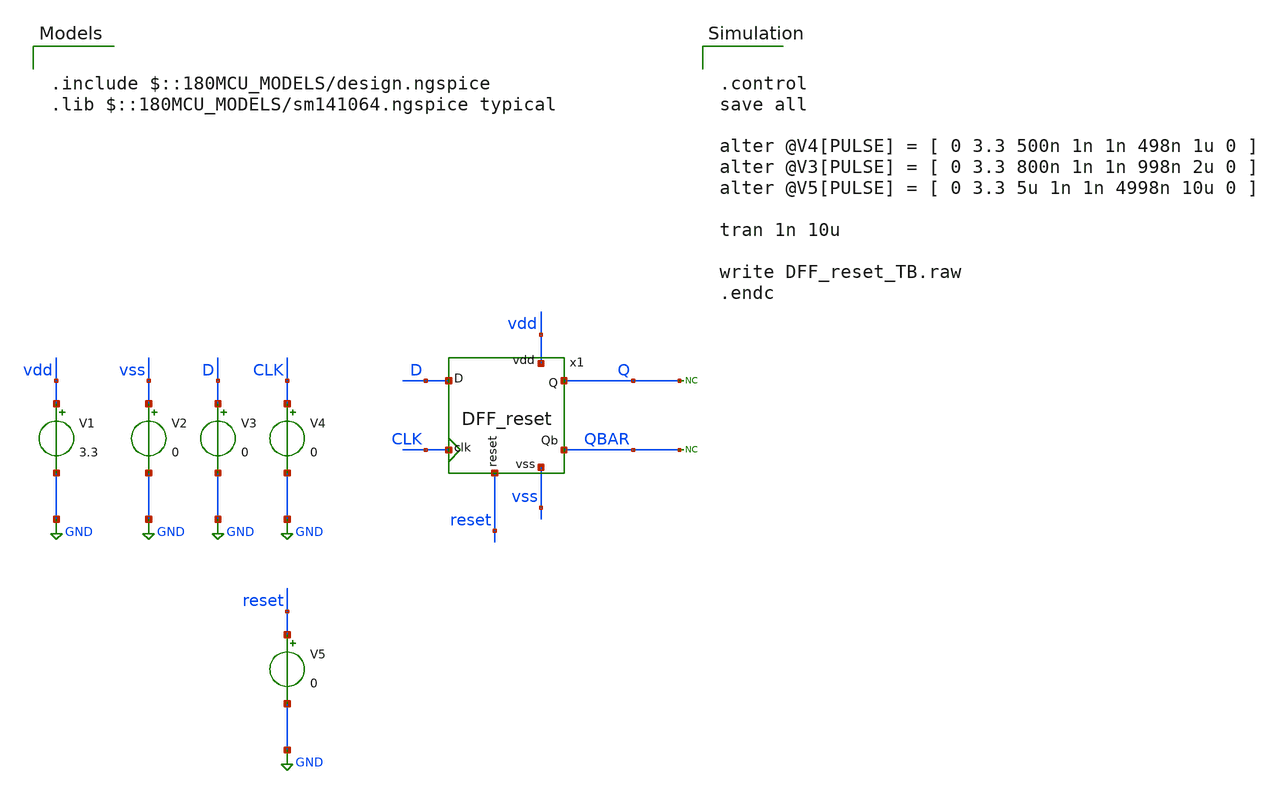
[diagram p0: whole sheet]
** sch_path: designs/libs/xp_tb_analog/tb_DFF_reset/DFF_reset_TB.sch
**.subckt DFF_reset_TB
x1 D Q vdd vss reset QBAR CLK DFF_reset
V1 vdd GND 3.3
V2 vss GND 0
* noconn Q
* noconn QBAR
V3 D GND 0
V4 CLK GND 0
V5 reset GND 0
**** begin user architecture code


.control
save all

alter @V4[PULSE] = [ 0 3.3 500n 1n 1n 498n 1u 0 ]
alter @V3[PULSE] = [ 0 3.3 800n 1n 1n 998n 2u 0 ]
alter @V5[PULSE] = [ 0 3.3 5u 1n 1n 4998n 10u 0 ]

tran 1n 10u

write DFF_reset_TB.raw
.endc



.include $::180MCU_MODELS/design.ngspice
.lib $::180MCU_MODELS/sm141064.ngspice typical

**** end user architecture code
**.ends
.GLOBAL GND
.end
